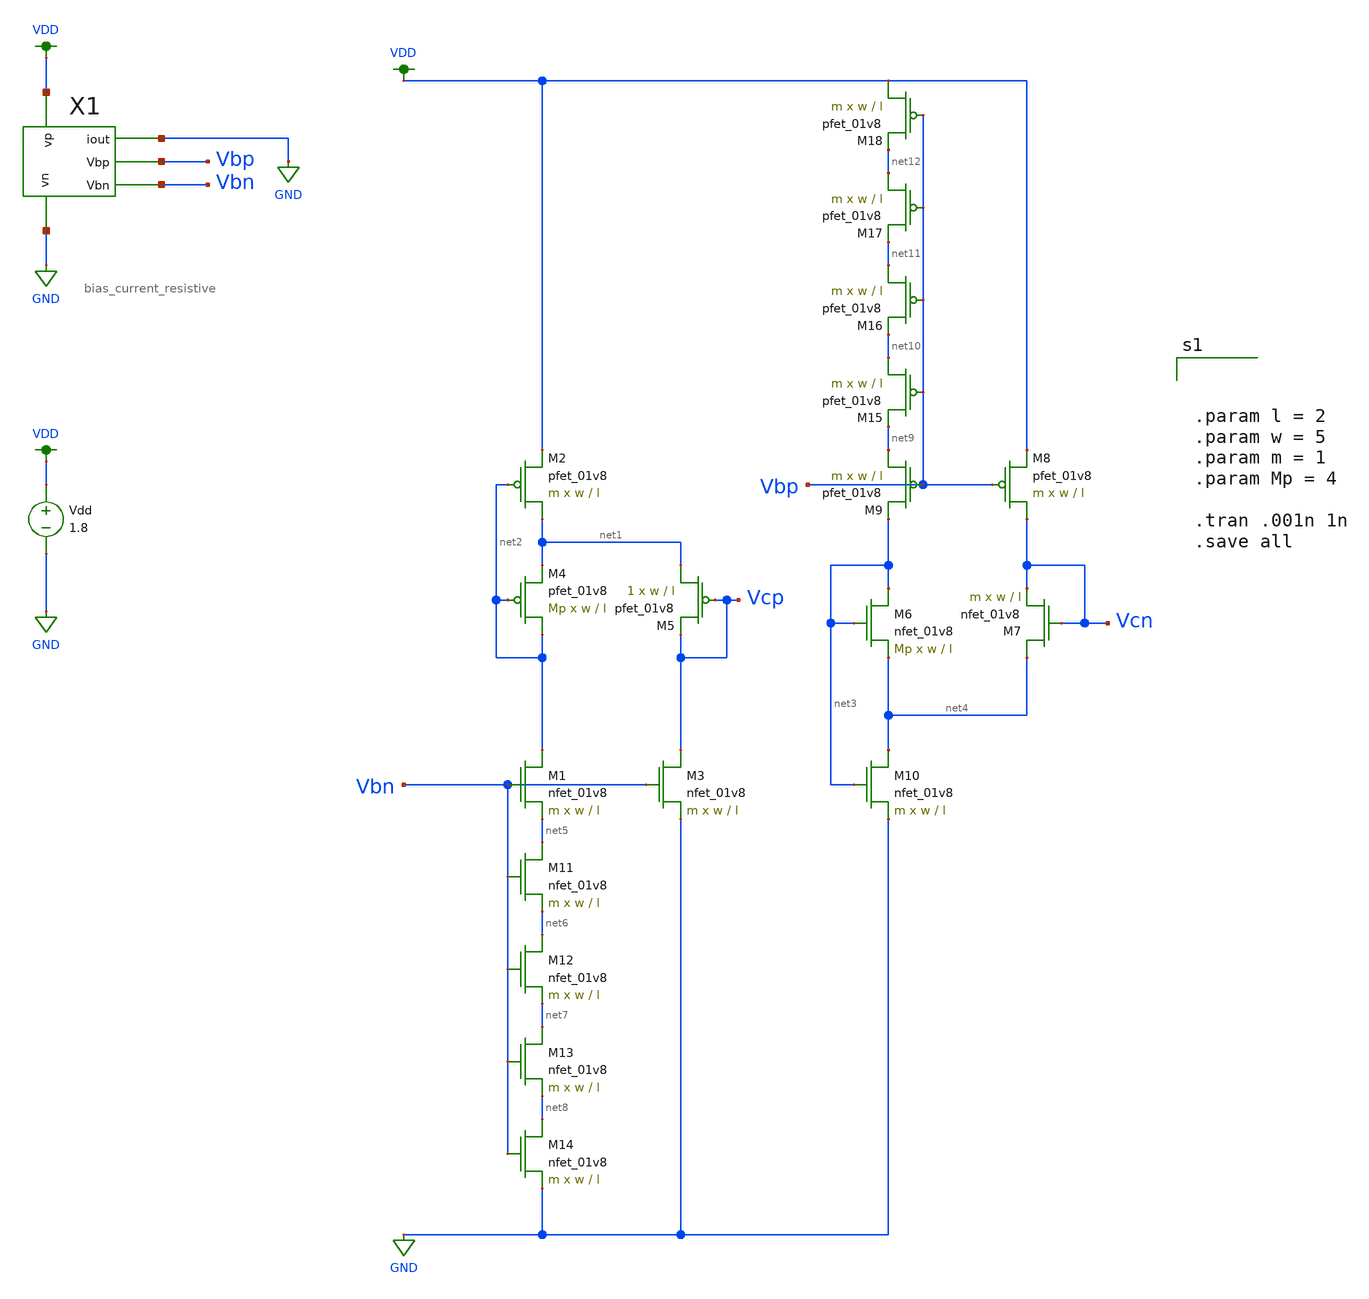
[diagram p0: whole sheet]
** sch_path: schematic/test/cascode_generator.sch
**.subckt cascode_generator
XM1 net2 Vbn net5 GND sky130_fd_pr__nfet_01v8 L=l W=w nf=1 ad='int((nf+1)/2) * W/nf * 0.29' as='int((nf+2)/2) * W/nf * 0.29'
+ pd='2*int((nf+1)/2) * (W/nf + 0.29)' ps='2*int((nf+2)/2) * (W/nf + 0.29)' nrd='0.29 / W' nrs='0.29 / W'
+ sa=0 sb=0 sd=0 mult=m m=m
XM2 net1 net2 VDD VDD sky130_fd_pr__pfet_01v8 L=l W=w nf=1 ad='int((nf+1)/2) * W/nf * 0.29' as='int((nf+2)/2) * W/nf * 0.29'
+ pd='2*int((nf+1)/2) * (W/nf + 0.29)' ps='2*int((nf+2)/2) * (W/nf + 0.29)' nrd='0.29 / W' nrs='0.29 / W'
+ sa=0 sb=0 sd=0 mult=m m=m
XM3 Vcp Vbn GND GND sky130_fd_pr__nfet_01v8 L=l W=w nf=1 ad='int((nf+1)/2) * W/nf * 0.29' as='int((nf+2)/2) * W/nf * 0.29'
+ pd='2*int((nf+1)/2) * (W/nf + 0.29)' ps='2*int((nf+2)/2) * (W/nf + 0.29)' nrd='0.29 / W' nrs='0.29 / W'
+ sa=0 sb=0 sd=0 mult=m m=m
XM4 net2 net2 net1 VDD sky130_fd_pr__pfet_01v8 L=l W=w nf=1 ad='int((nf+1)/2) * W/nf * 0.29' as='int((nf+2)/2) * W/nf * 0.29'
+ pd='2*int((nf+1)/2) * (W/nf + 0.29)' ps='2*int((nf+2)/2) * (W/nf + 0.29)' nrd='0.29 / W' nrs='0.29 / W'
+ sa=0 sb=0 sd=0 mult=Mp m=Mp
XM5 net1 Vcp Vcp VDD sky130_fd_pr__pfet_01v8 L=l W=w nf=1 ad='int((nf+1)/2) * W/nf * 0.29' as='int((nf+2)/2) * W/nf * 0.29'
+ pd='2*int((nf+1)/2) * (W/nf + 0.29)' ps='2*int((nf+2)/2) * (W/nf + 0.29)' nrd='0.29 / W' nrs='0.29 / W'
+ sa=0 sb=0 sd=0 mult=1 m=1
XM6 net3 net3 net4 GND sky130_fd_pr__nfet_01v8 L=l W=w nf=1 ad='int((nf+1)/2) * W/nf * 0.29' as='int((nf+2)/2) * W/nf * 0.29'
+ pd='2*int((nf+1)/2) * (W/nf + 0.29)' ps='2*int((nf+2)/2) * (W/nf + 0.29)' nrd='0.29 / W' nrs='0.29 / W'
+ sa=0 sb=0 sd=0 mult=Mp m=Mp
XM7 net4 Vcn Vcn GND sky130_fd_pr__nfet_01v8 L=l W=w nf=1 ad='int((nf+1)/2) * W/nf * 0.29' as='int((nf+2)/2) * W/nf * 0.29'
+ pd='2*int((nf+1)/2) * (W/nf + 0.29)' ps='2*int((nf+2)/2) * (W/nf + 0.29)' nrd='0.29 / W' nrs='0.29 / W'
+ sa=0 sb=0 sd=0 mult=m m=m
XM8 Vcn Vbp VDD VDD sky130_fd_pr__pfet_01v8 L=l W=w nf=1 ad='int((nf+1)/2) * W/nf * 0.29' as='int((nf+2)/2) * W/nf * 0.29'
+ pd='2*int((nf+1)/2) * (W/nf + 0.29)' ps='2*int((nf+2)/2) * (W/nf + 0.29)' nrd='0.29 / W' nrs='0.29 / W'
+ sa=0 sb=0 sd=0 mult=m m=m
XM9 net9 Vbp net3 VDD sky130_fd_pr__pfet_01v8 L=l W=w nf=1 ad='int((nf+1)/2) * W/nf * 0.29' as='int((nf+2)/2) * W/nf * 0.29'
+ pd='2*int((nf+1)/2) * (W/nf + 0.29)' ps='2*int((nf+2)/2) * (W/nf + 0.29)' nrd='0.29 / W' nrs='0.29 / W'
+ sa=0 sb=0 sd=0 mult=m m=m
XM10 net4 net3 GND GND sky130_fd_pr__nfet_01v8 L=l W=w nf=1 ad='int((nf+1)/2) * W/nf * 0.29' as='int((nf+2)/2) * W/nf * 0.29'
+ pd='2*int((nf+1)/2) * (W/nf + 0.29)' ps='2*int((nf+2)/2) * (W/nf + 0.29)' nrd='0.29 / W' nrs='0.29 / W'
+ sa=0 sb=0 sd=0 mult=m m=m
XM11 net5 Vbn net6 GND sky130_fd_pr__nfet_01v8 L=l W=w nf=1 ad='int((nf+1)/2) * W/nf * 0.29' as='int((nf+2)/2) * W/nf * 0.29'
+ pd='2*int((nf+1)/2) * (W/nf + 0.29)' ps='2*int((nf+2)/2) * (W/nf + 0.29)' nrd='0.29 / W' nrs='0.29 / W'
+ sa=0 sb=0 sd=0 mult=m m=m
XM12 net6 Vbn net7 GND sky130_fd_pr__nfet_01v8 L=l W=w nf=1 ad='int((nf+1)/2) * W/nf * 0.29' as='int((nf+2)/2) * W/nf * 0.29'
+ pd='2*int((nf+1)/2) * (W/nf + 0.29)' ps='2*int((nf+2)/2) * (W/nf + 0.29)' nrd='0.29 / W' nrs='0.29 / W'
+ sa=0 sb=0 sd=0 mult=m m=m
XM13 net7 Vbn net8 GND sky130_fd_pr__nfet_01v8 L=l W=w nf=1 ad='int((nf+1)/2) * W/nf * 0.29' as='int((nf+2)/2) * W/nf * 0.29'
+ pd='2*int((nf+1)/2) * (W/nf + 0.29)' ps='2*int((nf+2)/2) * (W/nf + 0.29)' nrd='0.29 / W' nrs='0.29 / W'
+ sa=0 sb=0 sd=0 mult=m m=m
XM14 net8 Vbn GND GND sky130_fd_pr__nfet_01v8 L=l W=w nf=1 ad='int((nf+1)/2) * W/nf * 0.29' as='int((nf+2)/2) * W/nf * 0.29'
+ pd='2*int((nf+1)/2) * (W/nf + 0.29)' ps='2*int((nf+2)/2) * (W/nf + 0.29)' nrd='0.29 / W' nrs='0.29 / W'
+ sa=0 sb=0 sd=0 mult=m m=m
XM15 net10 Vbp net9 VDD sky130_fd_pr__pfet_01v8 L=l W=w nf=1 ad='int((nf+1)/2) * W/nf * 0.29' as='int((nf+2)/2) * W/nf * 0.29'
+ pd='2*int((nf+1)/2) * (W/nf + 0.29)' ps='2*int((nf+2)/2) * (W/nf + 0.29)' nrd='0.29 / W' nrs='0.29 / W'
+ sa=0 sb=0 sd=0 mult=m m=m
XM16 net11 Vbp net10 VDD sky130_fd_pr__pfet_01v8 L=l W=w nf=1 ad='int((nf+1)/2) * W/nf * 0.29' as='int((nf+2)/2) * W/nf * 0.29'
+ pd='2*int((nf+1)/2) * (W/nf + 0.29)' ps='2*int((nf+2)/2) * (W/nf + 0.29)' nrd='0.29 / W' nrs='0.29 / W'
+ sa=0 sb=0 sd=0 mult=m m=m
XM17 net12 Vbp net11 VDD sky130_fd_pr__pfet_01v8 L=l W=w nf=1 ad='int((nf+1)/2) * W/nf * 0.29' as='int((nf+2)/2) * W/nf * 0.29'
+ pd='2*int((nf+1)/2) * (W/nf + 0.29)' ps='2*int((nf+2)/2) * (W/nf + 0.29)' nrd='0.29 / W' nrs='0.29 / W'
+ sa=0 sb=0 sd=0 mult=m m=m
XM18 VDD Vbp net12 VDD sky130_fd_pr__pfet_01v8 L=l W=w nf=1 ad='int((nf+1)/2) * W/nf * 0.29' as='int((nf+2)/2) * W/nf * 0.29'
+ pd='2*int((nf+1)/2) * (W/nf + 0.29)' ps='2*int((nf+2)/2) * (W/nf + 0.29)' nrd='0.29 / W' nrs='0.29 / W'
+ sa=0 sb=0 sd=0 mult=m m=m
Vdd VDD GND 1.8
X1 VDD GND GND Vbp Vbn bias_current_resistive
**** begin user architecture code

.option wnflag=1
.param MC_SWITCH=0.0
.lib ~/skywater/skywater-pdk/libraries/sky130_fd_pr_ngspice/latest/models/sky130.lib.spice tt




.param l = 2
.param w = 5
.param m = 1
.param Mp = 4

.tran .001n 1n
.save all


**** end user architecture code
**.ends

* expanding   symbol:
*+  /home/madvlsi/Desktop/madvlsi/madvlsi_proj_4/schematic/bias_current_resistive.sym # of pins=5
** sym_path: schematic/bias_current_resistive.sym
** sch_path: schematic/bias_current_resistive.sch
.subckt bias_current_resistive vp vn iout Vbp Vbn
*.iopin vp
*.iopin vn
*.opin iout
*.opin Vbp
*.opin Vbn
XM1 vp Vbp net2 VDD sky130_fd_pr__pfet_01v8 L=l W=w nf=1 ad='int((nf+1)/2) * W/nf * 0.29' as='int((nf+2)/2) * W/nf * 0.29'
+ pd='2*int((nf+1)/2) * (W/nf + 0.29)' ps='2*int((nf+2)/2) * (W/nf + 0.29)' nrd='0.29 / W' nrs='0.29 / W'
+ sa=0 sb=0 sd=0 mult=1 m=1
XM2 vp net3 net3 VDD sky130_fd_pr__pfet_01v8 L=l W=w nf=1 ad='int((nf+1)/2) * W/nf * 0.29' as='int((nf+2)/2) * W/nf * 0.29'
+ pd='2*int((nf+1)/2) * (W/nf + 0.29)' ps='2*int((nf+2)/2) * (W/nf + 0.29)' nrd='0.29 / W' nrs='0.29 / W'
+ sa=0 sb=0 sd=0 mult=1 m=1
XM3 Vbp net3 vp VDD sky130_fd_pr__pfet_01v8 L=l W=w nf=1 ad='int((nf+1)/2) * W/nf * 0.29' as='int((nf+2)/2) * W/nf * 0.29'
+ pd='2*int((nf+1)/2) * (W/nf + 0.29)' ps='2*int((nf+2)/2) * (W/nf + 0.29)' nrd='0.29 / W' nrs='0.29 / W'
+ sa=0 sb=0 sd=0 mult=1 m=1
XM5 Vbn Vbp vp VDD sky130_fd_pr__pfet_01v8 L=l W=w nf=1 ad='int((nf+1)/2) * W/nf * 0.29' as='int((nf+2)/2) * W/nf * 0.29'
+ pd='2*int((nf+1)/2) * (W/nf + 0.29)' ps='2*int((nf+2)/2) * (W/nf + 0.29)' nrd='0.29 / W' nrs='0.29 / W'
+ sa=0 sb=0 sd=0 mult=1 m=1
XM4 net1 net2 net2 GND sky130_fd_pr__nfet_01v8 L=l W=w nf=1 ad='int((nf+1)/2) * W/nf * 0.29' as='int((nf+2)/2) * W/nf * 0.29'
+ pd='2*int((nf+1)/2) * (W/nf + 0.29)' ps='2*int((nf+2)/2) * (W/nf + 0.29)' nrd='0.29 / W' nrs='0.29 / W'
+ sa=0 sb=0 sd=0 mult=Mn m=Mn
XM6 net3 net2 vn GND sky130_fd_pr__nfet_01v8 L=l W=w nf=1 ad='int((nf+1)/2) * W/nf * 0.29' as='int((nf+2)/2) * W/nf * 0.29'
+ pd='2*int((nf+1)/2) * (W/nf + 0.29)' ps='2*int((nf+2)/2) * (W/nf + 0.29)' nrd='0.29 / W' nrs='0.29 / W'
+ sa=0 sb=0 sd=0 mult=1 m=1
XM7 vn Vbn Vbp GND sky130_fd_pr__nfet_01v8 L=l W=w nf=1 ad='int((nf+1)/2) * W/nf * 0.29' as='int((nf+2)/2) * W/nf * 0.29'
+ pd='2*int((nf+1)/2) * (W/nf + 0.29)' ps='2*int((nf+2)/2) * (W/nf + 0.29)' nrd='0.29 / W' nrs='0.29 / W'
+ sa=0 sb=0 sd=0 mult=1 m=1
XM8 Vbn Vbn vn GND sky130_fd_pr__nfet_01v8 L=l W=w nf=1 ad='int((nf+1)/2) * W/nf * 0.29' as='int((nf+2)/2) * W/nf * 0.29'
+ pd='2*int((nf+1)/2) * (W/nf + 0.29)' ps='2*int((nf+2)/2) * (W/nf + 0.29)' nrd='0.29 / W' nrs='0.29 / W'
+ sa=0 sb=0 sd=0 mult=1 m=1
R1 net1 vn 74k m=1
**** begin user architecture code


.param w=5
.param l=2
.param Mn=8


**** end user architecture code
XM9 iout Vbp vp VDD sky130_fd_pr__pfet_01v8 L=l W=w nf=1 ad='int((nf+1)/2) * W/nf * 0.29' as='int((nf+2)/2) * W/nf * 0.29'
+ pd='2*int((nf+1)/2) * (W/nf + 0.29)' ps='2*int((nf+2)/2) * (W/nf + 0.29)' nrd='0.29 / W' nrs='0.29 / W'
+ sa=0 sb=0 sd=0 mult=1 m=1
.ends

.GLOBAL VDD
.GLOBAL GND
.end
